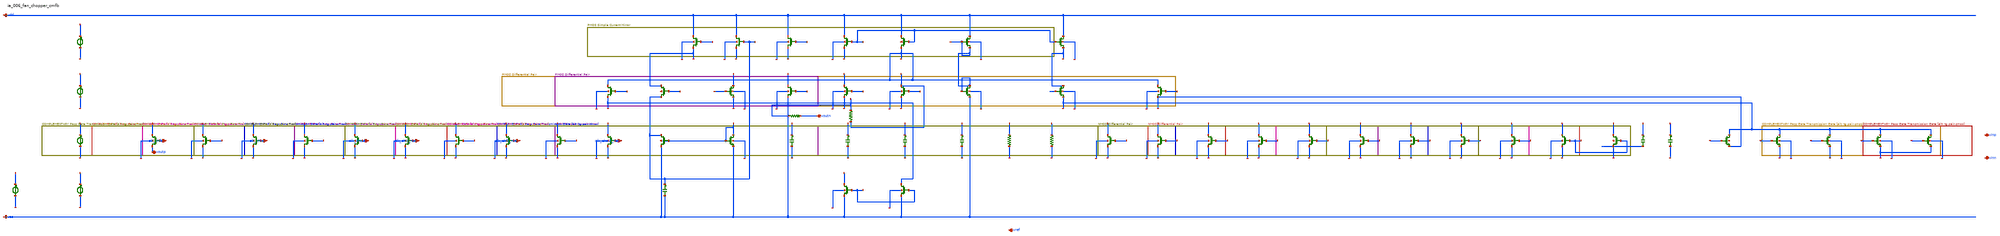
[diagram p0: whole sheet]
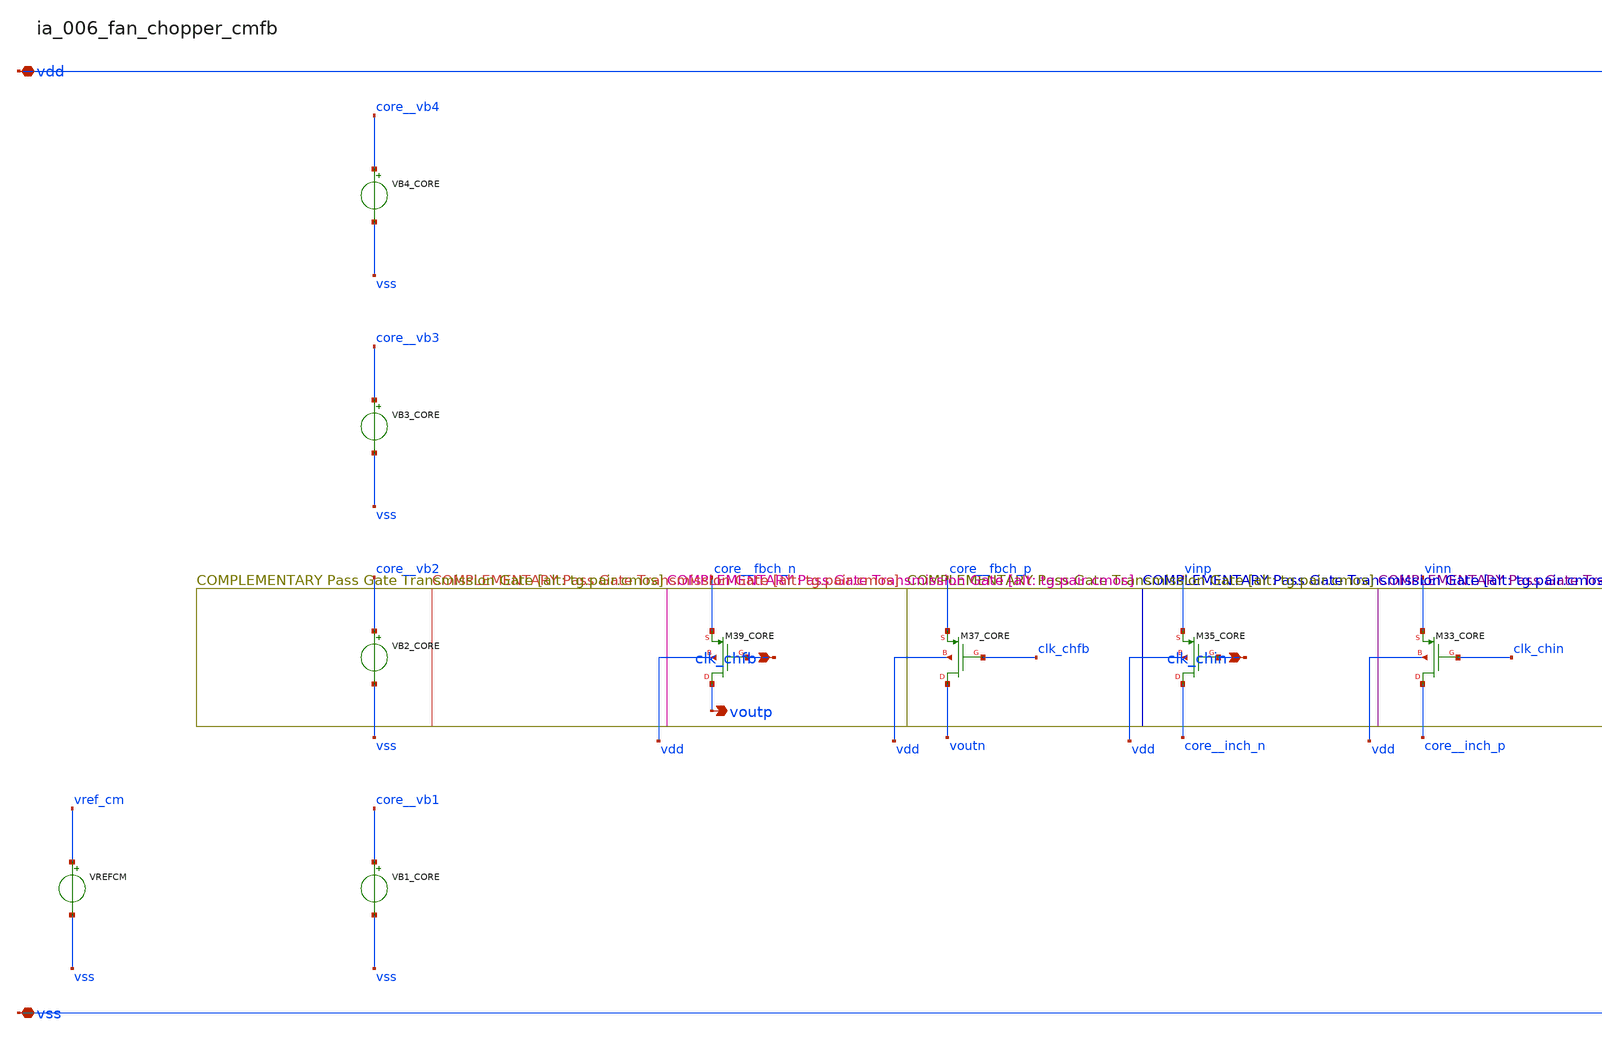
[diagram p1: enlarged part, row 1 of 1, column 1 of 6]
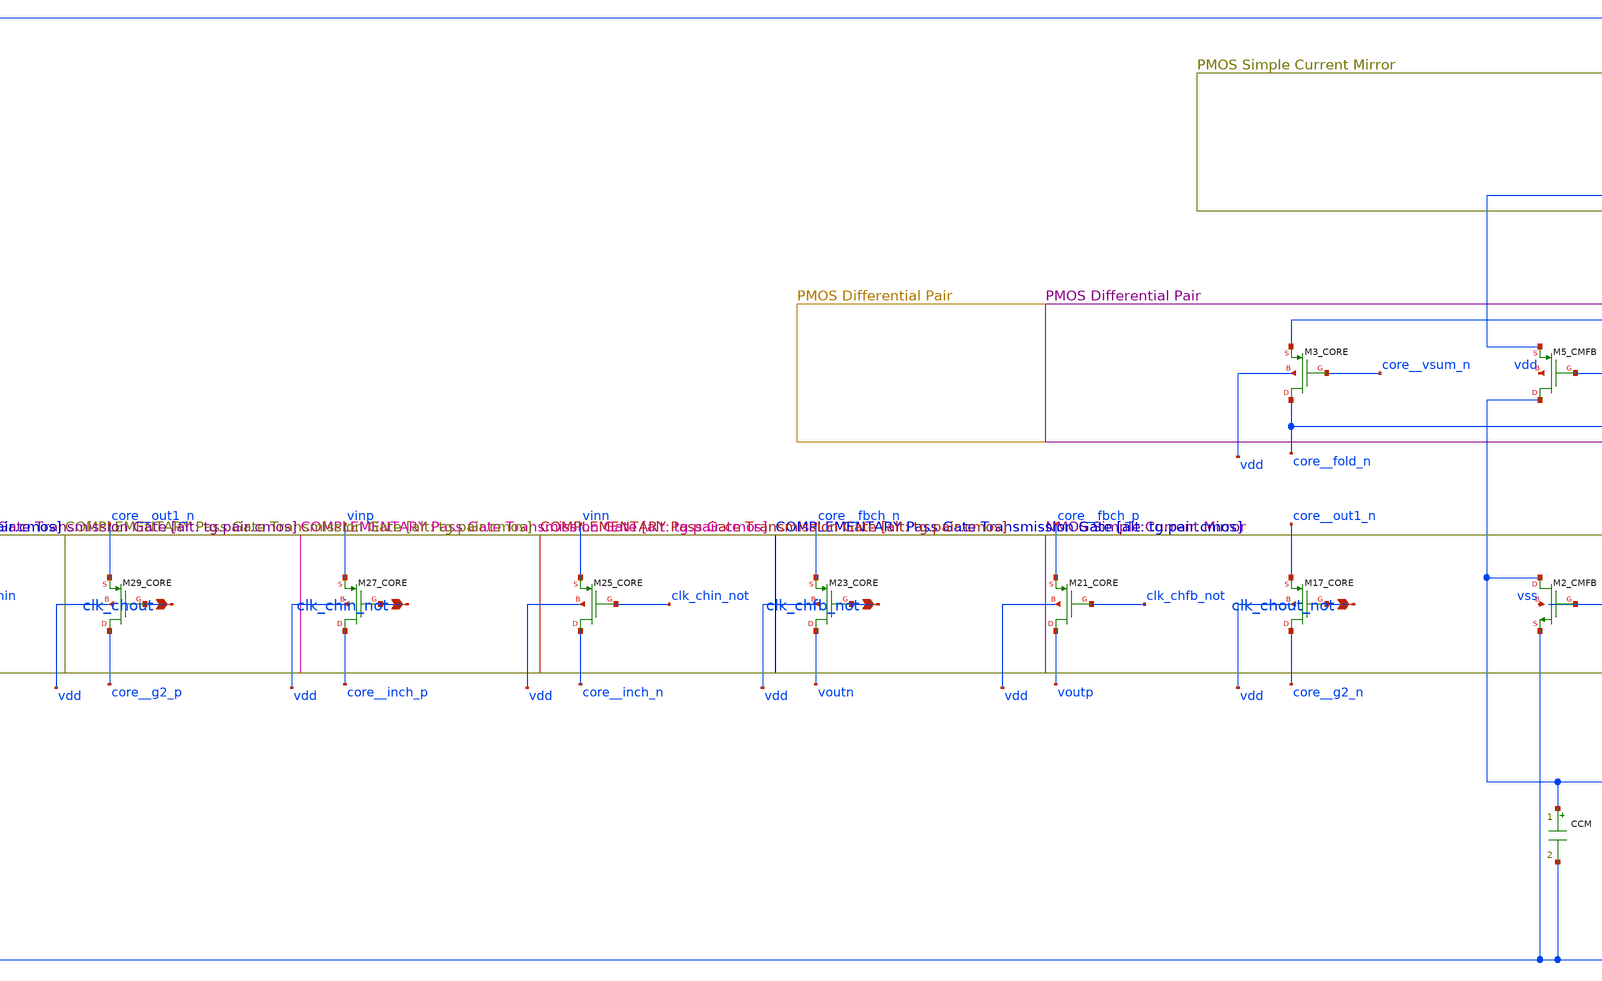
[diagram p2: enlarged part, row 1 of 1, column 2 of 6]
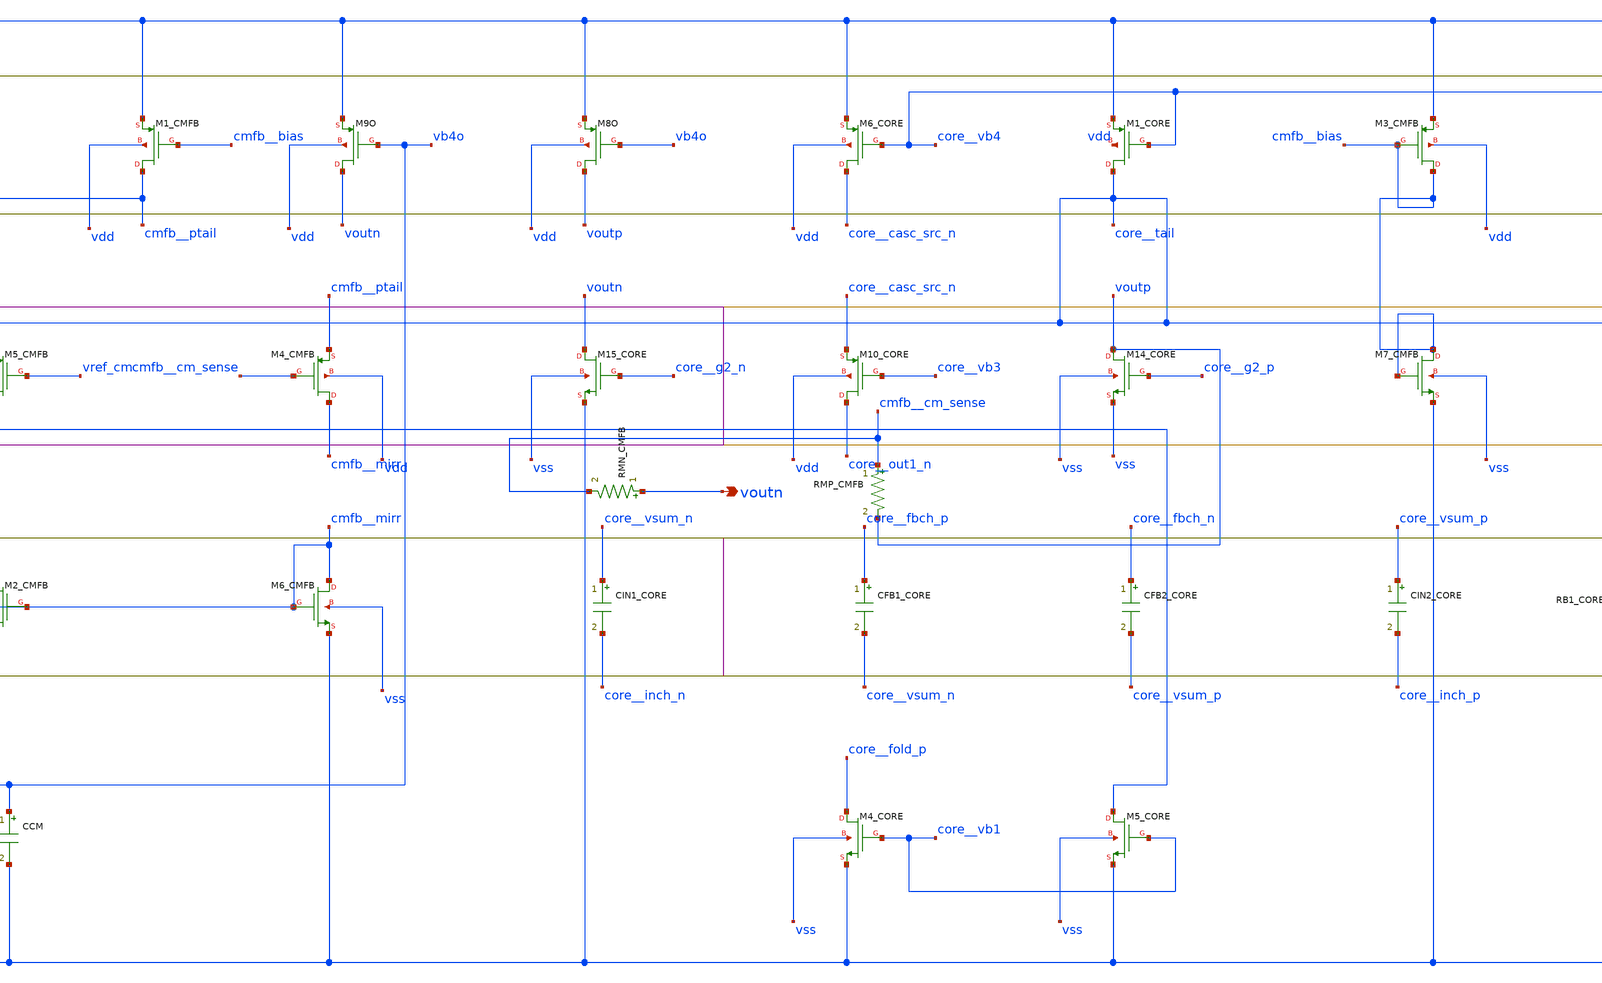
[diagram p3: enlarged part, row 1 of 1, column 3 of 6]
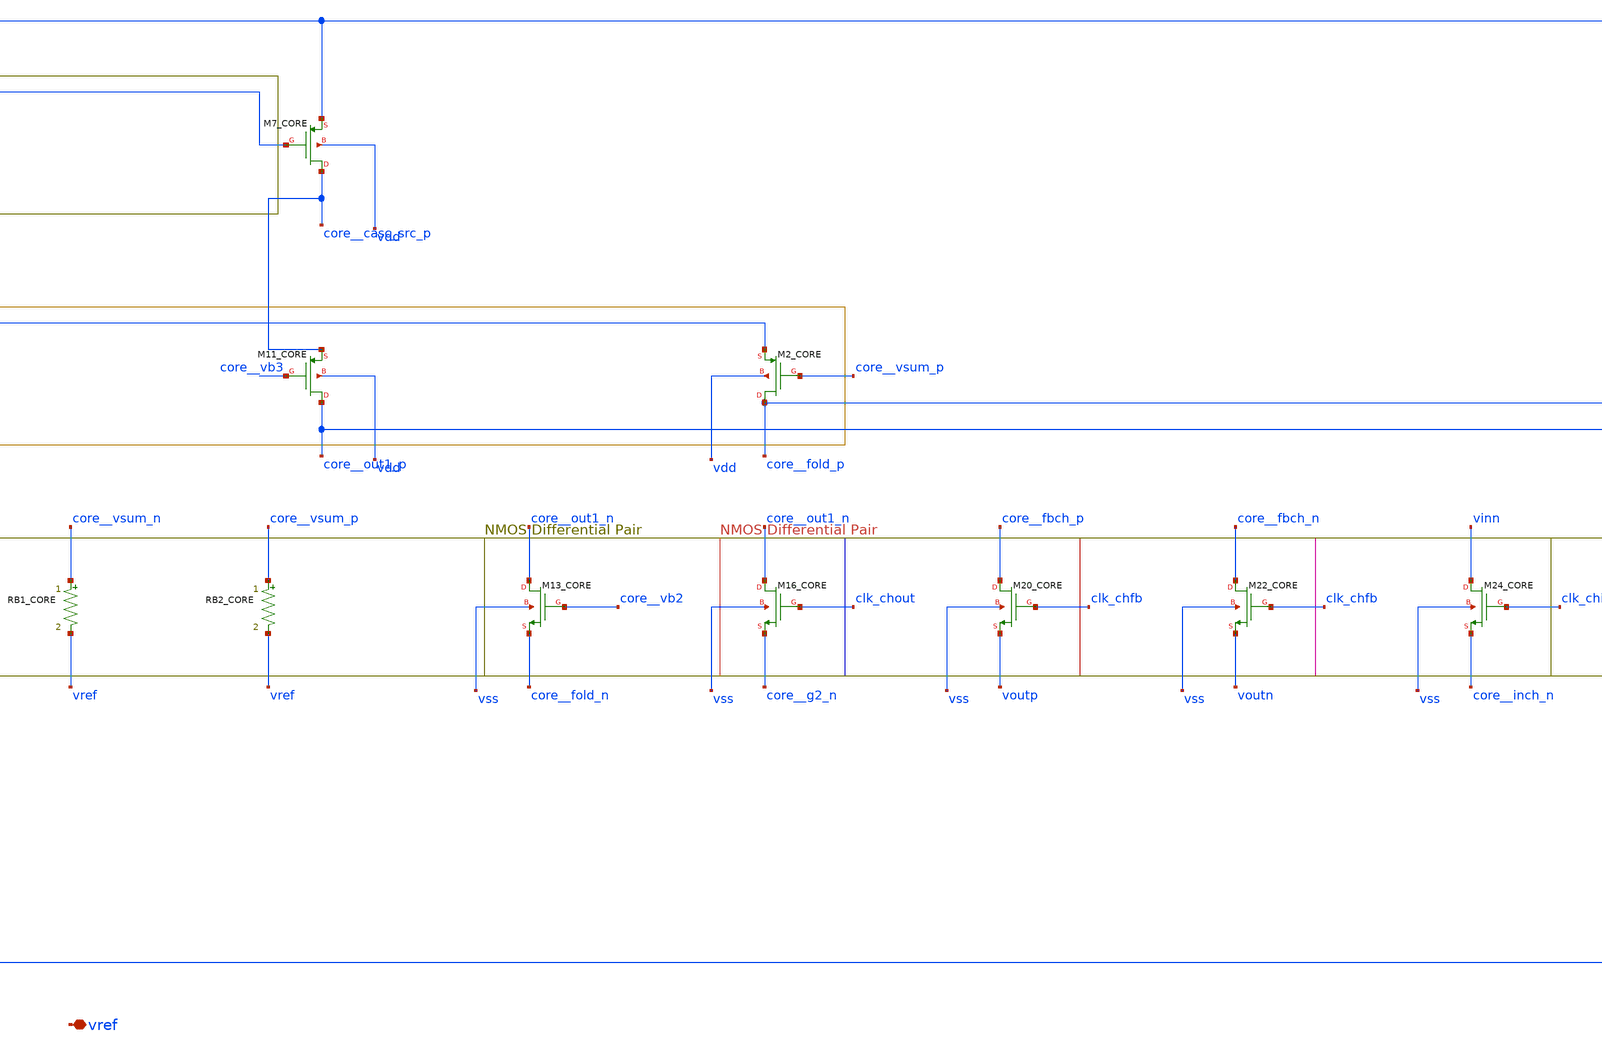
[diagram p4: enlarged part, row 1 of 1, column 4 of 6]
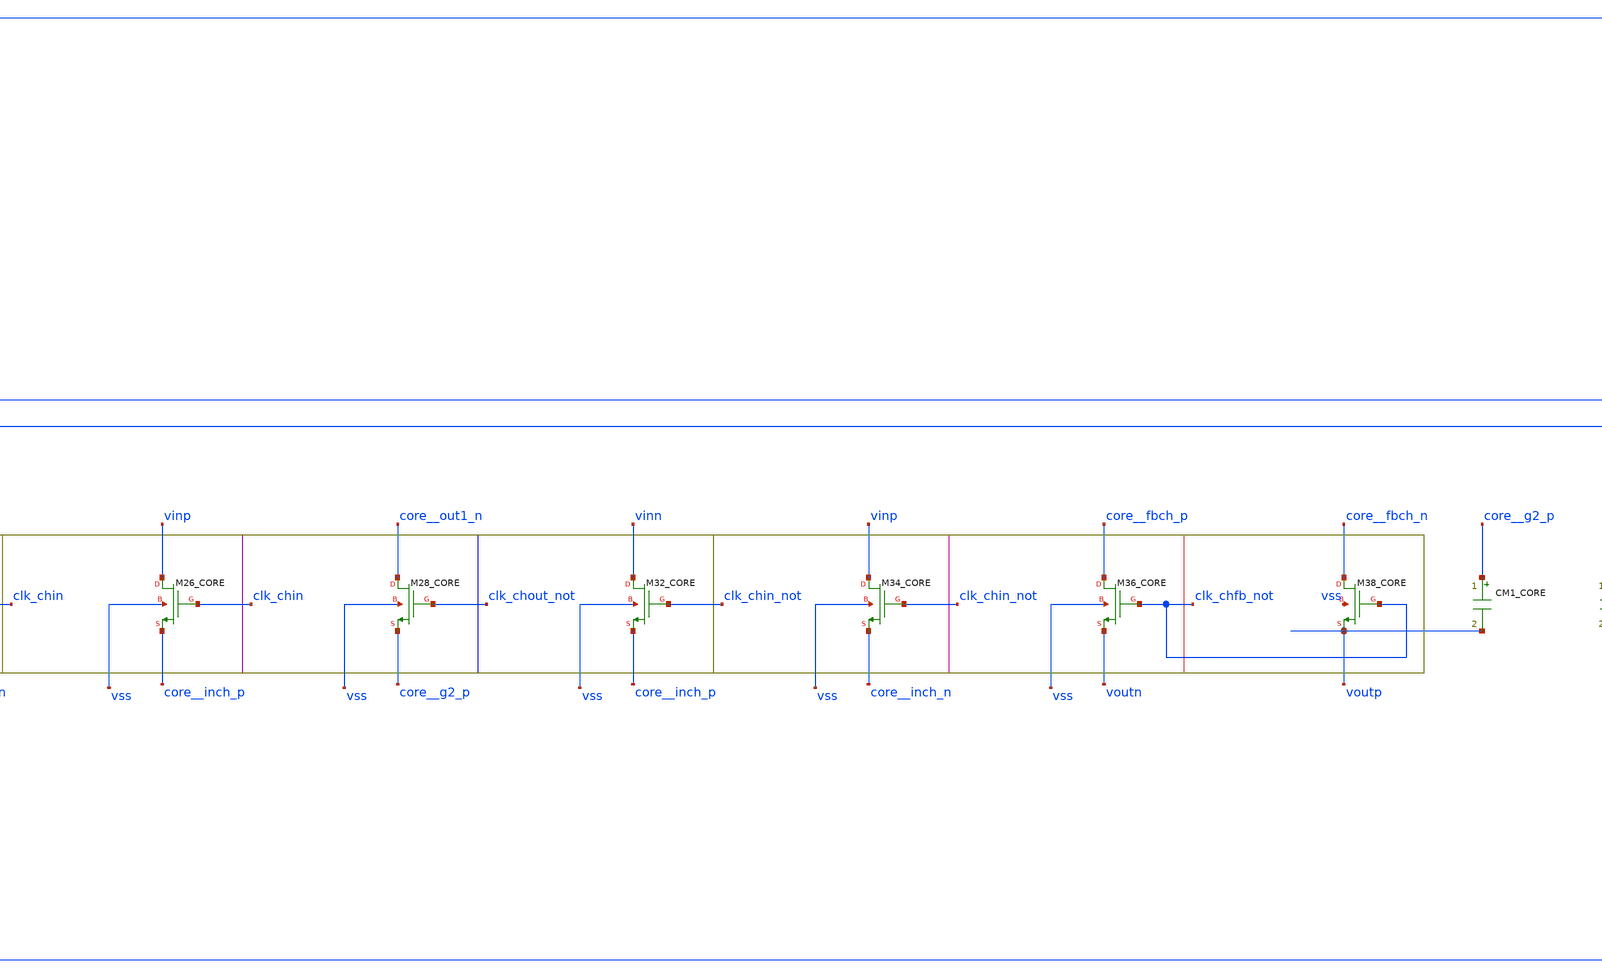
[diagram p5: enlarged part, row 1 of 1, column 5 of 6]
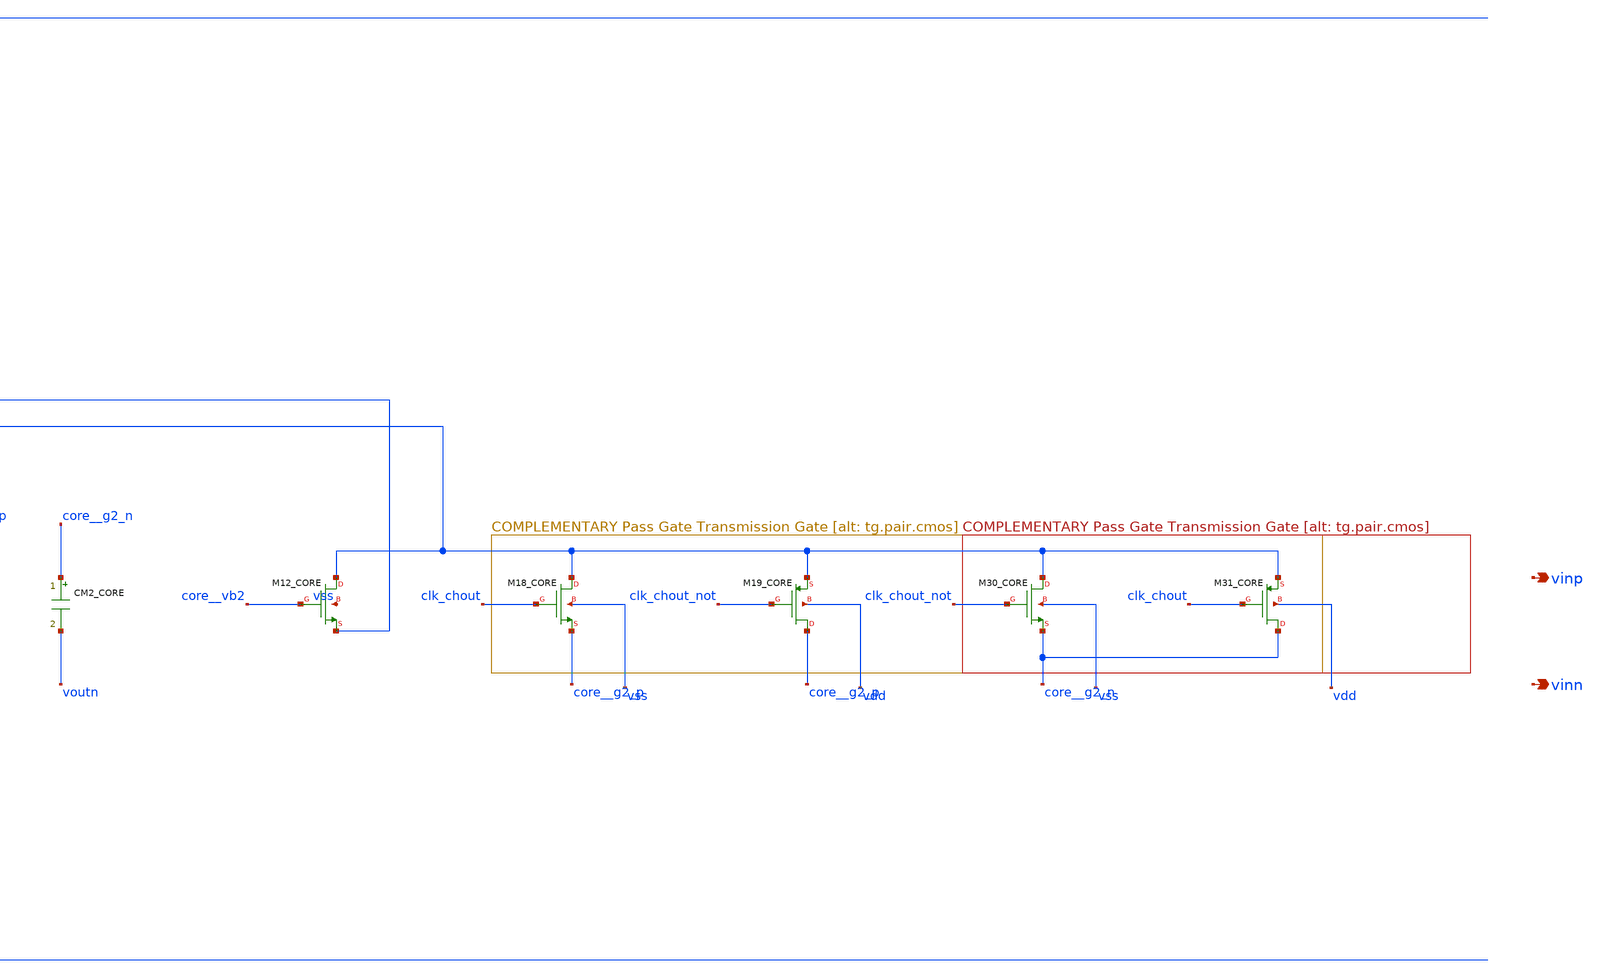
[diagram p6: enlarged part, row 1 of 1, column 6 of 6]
** sch_path: analog-db/raw/ia_006_fan_chopper_cmfb/ia_006_fan_chopper_cmfb_annotated.sch
**.subckt ia_006_fan_chopper_cmfb_annotated clk_chfb clk_chin clk_chout clk_chin_not clk_chfb_not
*+ clk_chout_not vdd vss voutn voutp vref vinp vinn
*.ipin clk_chfb
*.ipin clk_chin
*.ipin clk_chout
*.ipin clk_chin_not
*.ipin clk_chfb_not
*.ipin clk_chout_not
*.iopin vdd
*.iopin vss
*.opin voutn
*.opin voutp
*.iopin vref
*.opin vinp
*.opin vinn
CCM vb4o vss 'c_cm' m=1
CFB1_CORE core__fbch_p core__vsum_n 'x_dut_cfb1_core_value' m=1
CFB2_CORE core__fbch_n core__vsum_p 'x_dut_cfb2_core_value' m=1
CIN1_CORE core__vsum_n core__inch_n 'x_dut_cin1_core_value' m=1
CIN2_CORE core__vsum_p core__inch_p 'x_dut_cin2_core_value' m=1
CM1_CORE core__g2_p voutp 'x_dut_cm1_core_value' m=1
CM2_CORE core__g2_n voutn 'x_dut_cm2_core_value' m=1
RB1_CORE core__vsum_n vref 'x_dut_rb1_core_value' m=1
RB2_CORE core__vsum_p vref 'x_dut_rb2_core_value' m=1
RMN_CMFB voutn cmfb__cm_sense 'x_dut_rmn_cmfb_value' m=1
RMP_CMFB cmfb__cm_sense voutp 'x_dut_rmp_cmfb_value' m=1
VB1_CORE core__vb1 vss dc {vb1_core}
VB2_CORE core__vb2 vss dc {vb2_core}
VB3_CORE core__vb3 vss dc {vb3_core}
VB4_CORE core__vb4 vss dc {vb4_core}
VREFCM vref_cm vss dc {vcm_ref}
XM10_CORE core__out1_n core__vb3 core__casc_src_n vdd sg13_lv_pmos w=x_dut_xm10_core_w
+ l=x_dut_xm10_core_l ng=1 m=x_dut_xm10_core_m
XM11_CORE core__out1_p core__vb3 core__casc_src_p vdd sg13_lv_pmos w=x_dut_xm11_core_w
+ l=x_dut_xm11_core_l ng=1 m=x_dut_xm11_core_m
XM12_CORE core__out1_p core__vb2 core__fold_p vss sg13_lv_nmos w=x_dut_xm12_core_w
+ l=x_dut_xm12_core_l ng=1 m=x_dut_xm12_core_m
XM13_CORE core__out1_n core__vb2 core__fold_n vss sg13_lv_nmos w=x_dut_xm13_core_w
+ l=x_dut_xm13_core_l ng=1 m=x_dut_xm13_core_m
XM14_CORE voutp core__g2_p vss vss sg13_lv_nmos w=x_dut_xm14_core_w l=x_dut_xm14_core_l ng=1
+ m=x_dut_xm14_core_m
XM15_CORE voutn core__g2_n vss vss sg13_lv_nmos w=x_dut_xm15_core_w l=x_dut_xm15_core_l ng=1
+ m=x_dut_xm15_core_m
XM16_CORE core__out1_n clk_chout core__g2_n vss sg13_lv_nmos w=x_dut_xm16_core_w l=x_dut_xm16_core_l
+ ng=1 m=x_dut_xm16_core_m
XM17_CORE core__g2_n clk_chout_not core__out1_n vdd sg13_lv_pmos w=x_dut_xm17_core_w
+ l=x_dut_xm17_core_l ng=1 m=x_dut_xm17_core_m
XM18_CORE core__out1_p clk_chout core__g2_p vss sg13_lv_nmos w=x_dut_xm18_core_w l=x_dut_xm18_core_l
+ ng=1 m=x_dut_xm18_core_m
XM19_CORE core__g2_p clk_chout_not core__out1_p vdd sg13_lv_pmos w=x_dut_xm19_core_w
+ l=x_dut_xm19_core_l ng=1 m=x_dut_xm19_core_m
XM1_CMFB cmfb__ptail cmfb__bias vdd vdd sg13_lv_pmos w=x_dut_xm1_cmfb_w l=x_dut_xm1_cmfb_l ng=1
+ m=x_dut_xm1_cmfb_m
XM1_CORE core__tail core__vb4 vdd vdd sg13_lv_pmos w=x_dut_xm1_core_w l=x_dut_xm1_core_l ng=1
+ m=x_dut_xm1_core_m
XM20_CORE core__fbch_p clk_chfb voutp vss sg13_lv_nmos w=x_dut_xm20_core_w l=x_dut_xm20_core_l ng=1
+ m=x_dut_xm20_core_m
XM21_CORE voutp clk_chfb_not core__fbch_p vdd sg13_lv_pmos w=x_dut_xm21_core_w l=x_dut_xm21_core_l
+ ng=1 m=x_dut_xm21_core_m
XM22_CORE core__fbch_n clk_chfb voutn vss sg13_lv_nmos w=x_dut_xm22_core_w l=x_dut_xm22_core_l ng=1
+ m=x_dut_xm22_core_m
XM23_CORE voutn clk_chfb_not core__fbch_n vdd sg13_lv_pmos w=x_dut_xm23_core_w l=x_dut_xm23_core_l
+ ng=1 m=x_dut_xm23_core_m
XM24_CORE vinn clk_chin core__inch_n vss sg13_lv_nmos w=x_dut_xm24_core_w l=x_dut_xm24_core_l ng=1
+ m=x_dut_xm24_core_m
XM25_CORE core__inch_n clk_chin_not vinn vdd sg13_lv_pmos w=x_dut_xm25_core_w l=x_dut_xm25_core_l
+ ng=1 m=x_dut_xm25_core_m
XM26_CORE vinp clk_chin core__inch_p vss sg13_lv_nmos w=x_dut_xm26_core_w l=x_dut_xm26_core_l ng=1
+ m=x_dut_xm26_core_m
XM27_CORE core__inch_p clk_chin_not vinp vdd sg13_lv_pmos w=x_dut_xm27_core_w l=x_dut_xm27_core_l
+ ng=1 m=x_dut_xm27_core_m
XM28_CORE core__out1_n clk_chout_not core__g2_p vss sg13_lv_nmos w=x_dut_xm28_core_w
+ l=x_dut_xm28_core_l ng=1 m=x_dut_xm28_core_m
XM29_CORE core__g2_p clk_chout core__out1_n vdd sg13_lv_pmos w=x_dut_xm29_core_w l=x_dut_xm29_core_l
+ ng=1 m=x_dut_xm29_core_m
XM2_CMFB vb4o cmfb__mirr vss vss sg13_lv_nmos w=x_dut_xm2_cmfb_w l=x_dut_xm2_cmfb_l ng=1
+ m=x_dut_xm2_cmfb_m
XM2_CORE core__fold_p core__vsum_p core__tail vdd sg13_lv_pmos w=x_dut_xm2_core_w l=x_dut_xm2_core_l
+ ng=1 m=x_dut_xm2_core_m
XM30_CORE core__out1_p clk_chout_not core__g2_n vss sg13_lv_nmos w=x_dut_xm30_core_w
+ l=x_dut_xm30_core_l ng=1 m=x_dut_xm30_core_m
XM31_CORE core__g2_n clk_chout core__out1_p vdd sg13_lv_pmos w=x_dut_xm31_core_w l=x_dut_xm31_core_l
+ ng=1 m=x_dut_xm31_core_m
XM32_CORE vinn clk_chin_not core__inch_p vss sg13_lv_nmos w=x_dut_xm32_core_w l=x_dut_xm32_core_l
+ ng=1 m=x_dut_xm32_core_m
XM33_CORE core__inch_p clk_chin vinn vdd sg13_lv_pmos w=x_dut_xm33_core_w l=x_dut_xm33_core_l ng=1
+ m=x_dut_xm33_core_m
XM34_CORE vinp clk_chin_not core__inch_n vss sg13_lv_nmos w=x_dut_xm34_core_w l=x_dut_xm34_core_l
+ ng=1 m=x_dut_xm34_core_m
XM35_CORE core__inch_n clk_chin vinp vdd sg13_lv_pmos w=x_dut_xm35_core_w l=x_dut_xm35_core_l ng=1
+ m=x_dut_xm35_core_m
XM36_CORE core__fbch_p clk_chfb_not voutn vss sg13_lv_nmos w=x_dut_xm36_core_w l=x_dut_xm36_core_l
+ ng=1 m=x_dut_xm36_core_m
XM37_CORE voutn clk_chfb core__fbch_p vdd sg13_lv_pmos w=x_dut_xm37_core_w l=x_dut_xm37_core_l ng=1
+ m=x_dut_xm37_core_m
XM38_CORE core__fbch_n clk_chfb_not voutp vss sg13_lv_nmos w=x_dut_xm38_core_w l=x_dut_xm38_core_l
+ ng=1 m=x_dut_xm38_core_m
XM39_CORE voutp clk_chfb core__fbch_n vdd sg13_lv_pmos w=x_dut_xm39_core_w l=x_dut_xm39_core_l ng=1
+ m=x_dut_xm39_core_m
XM3_CMFB cmfb__bias cmfb__bias vdd vdd sg13_lv_pmos w=x_dut_xm3_cmfb_w l=x_dut_xm3_cmfb_l ng=1
+ m=x_dut_xm3_cmfb_m
XM3_CORE core__fold_n core__vsum_n core__tail vdd sg13_lv_pmos w=x_dut_xm3_core_w l=x_dut_xm3_core_l
+ ng=1 m=x_dut_xm3_core_m
XM4_CMFB cmfb__mirr cmfb__cm_sense cmfb__ptail vdd sg13_lv_pmos w=x_dut_xm4_cmfb_w
+ l=x_dut_xm4_cmfb_l ng=1 m=x_dut_xm4_cmfb_m
XM4_CORE core__fold_p core__vb1 vss vss sg13_lv_nmos w=x_dut_xm4_core_w l=x_dut_xm4_core_l ng=1
+ m=x_dut_xm4_core_m
XM5_CMFB vb4o vref_cm cmfb__ptail vdd sg13_lv_pmos w=x_dut_xm5_cmfb_w l=x_dut_xm5_cmfb_l ng=1
+ m=x_dut_xm5_cmfb_m
XM5_CORE core__fold_n core__vb1 vss vss sg13_lv_nmos w=x_dut_xm5_core_w l=x_dut_xm5_core_l ng=1
+ m=x_dut_xm5_core_m
XM6_CMFB cmfb__mirr cmfb__mirr vss vss sg13_lv_nmos w=x_dut_xm6_cmfb_w l=x_dut_xm6_cmfb_l ng=1
+ m=x_dut_xm6_cmfb_m
XM6_CORE core__casc_src_n core__vb4 vdd vdd sg13_lv_pmos w=x_dut_xm6_core_w l=x_dut_xm6_core_l ng=1
+ m=x_dut_xm6_core_m
XM7_CMFB cmfb__bias cmfb__bias vss vss sg13_lv_nmos w=x_dut_xm7_cmfb_w l=x_dut_xm7_cmfb_l ng=1
+ m=x_dut_xm7_cmfb_m
XM7_CORE core__casc_src_p core__vb4 vdd vdd sg13_lv_pmos w=x_dut_xm7_core_w l=x_dut_xm7_core_l ng=1
+ m=x_dut_xm7_core_m
XM8O voutp vb4o vdd vdd sg13_lv_pmos w=x_dut_xm8o_w l=x_dut_xm8o_l ng=1 m=x_dut_xm8o_m
XM9O voutn vb4o vdd vdd sg13_lv_pmos w=x_dut_xm9o_w l=x_dut_xm9o_l ng=1 m=x_dut_xm9o_m
**.ends
.end
